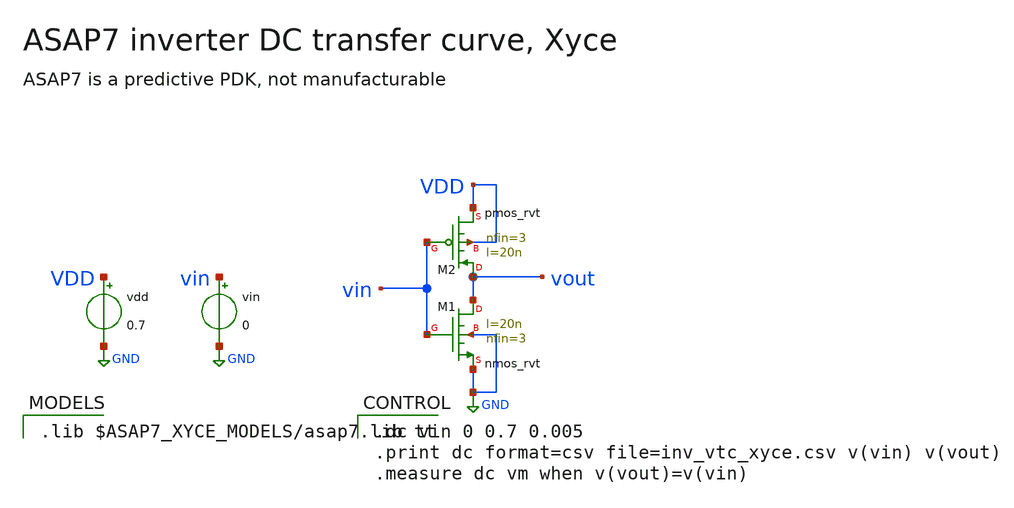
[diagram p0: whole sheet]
** sch_path: _build/images/open_pdks/asap7/libs.tech/xschem/asap7_tests/inv_vtc_xyce.sch
* SPDX-FileCopyrightText: 2026 Harald Pretl
* Johannes Kepler University, Department for Integrated Circuits
* SPDX-License-Identifier: Apache-2.0
**.subckt inv_vtc_xyce
XM2 vout vin VDD VDD pmos_rvt l=20n nfin=3 mm=0
XM1 vout vin GND GND nmos_rvt l=20n nfin=3 mm=0
vdd VDD GND 0.7
vin vin GND 0
**** begin user architecture code

.lib $ASAP7_XYCE_MODELS/asap7.lib tt



.dc vin 0 0.7 0.005
.print dc format=csv file=inv_vtc_xyce.csv v(vin) v(vout)
.measure dc vm when v(vout)=v(vin)


**** end user architecture code
**.ends
.GLOBAL GND
.end
